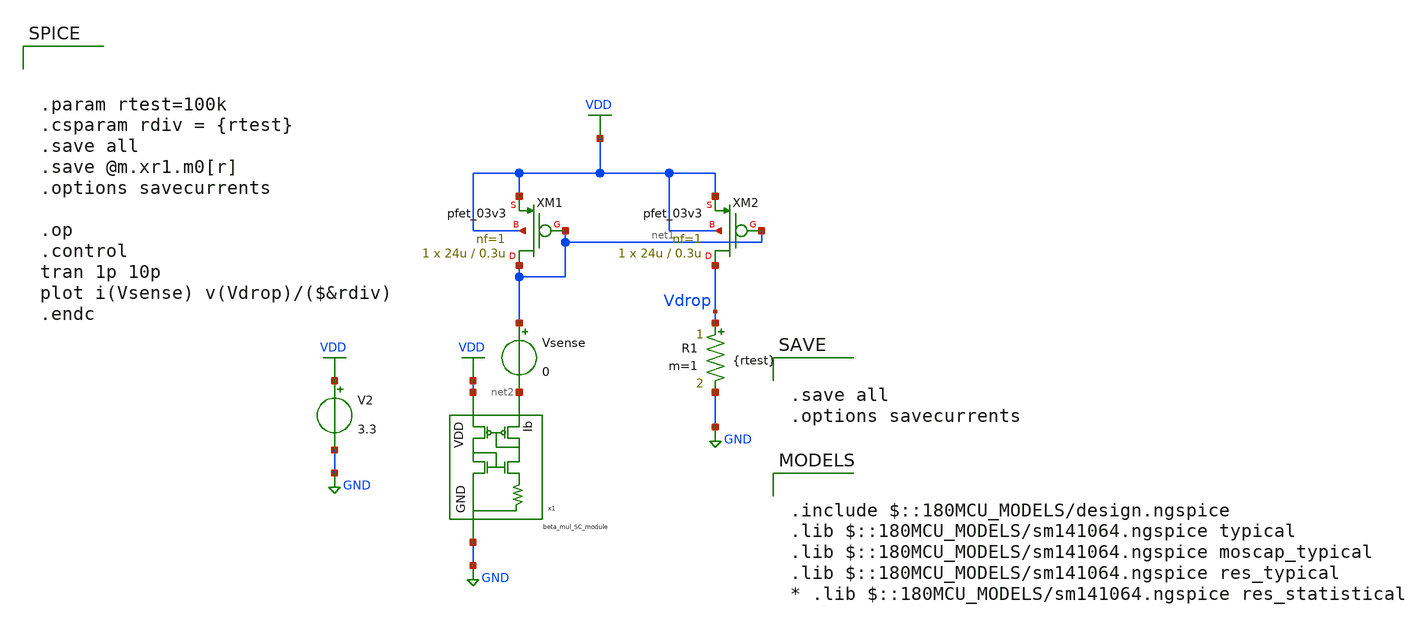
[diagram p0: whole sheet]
** sch_path: beta_mul_tb.sch
**.subckt beta_mul_tb
x1 VDD net2 GND beta_mul_SC_module
XM1 net1 net1 VDD VDD pfet_03v3 L=0.3u W=24u nf=1 ad='int((nf+1)/2) * W/nf * 0.18u' as='int((nf+2)/2) * W/nf * 0.18u'
+ pd='2*int((nf+1)/2) * (W/nf + 0.18u)' ps='2*int((nf+2)/2) * (W/nf + 0.18u)' nrd='0.18u / W' nrs='0.18u / W'
+ sa=0 sb=0 sd=0 m=1 par=1
XM2 Vdrop net1 VDD VDD pfet_03v3 L=0.3u W=24u nf=1 ad='int((nf+1)/2) * W/nf * 0.18u' as='int((nf+2)/2) * W/nf * 0.18u'
+ pd='2*int((nf+1)/2) * (W/nf + 0.18u)' ps='2*int((nf+2)/2) * (W/nf + 0.18u)' nrd='0.18u / W' nrs='0.18u / W'
+ sa=0 sb=0 sd=0 m=1 par=1
R1 Vdrop GND {rtest} m=1
Vsense net1 net2 0
V2 VDD GND 3.3
**** begin user architecture code

.include $::180MCU_MODELS/design.ngspice
.lib $::180MCU_MODELS/sm141064.ngspice typical
.lib $::180MCU_MODELS/sm141064.ngspice moscap_typical
.lib $::180MCU_MODELS/sm141064.ngspice res_typical
* .lib $::180MCU_MODELS/sm141064.ngspice res_statistical



.save all
.options savecurrents





.param rtest=100k
.csparam rdiv = {rtest}
.save all
.save @m.xr1.m0[r]
.options savecurrents

.op
.control
tran 1p 10p
plot i(Vsense) v(Vdrop)/($&rdiv)
.endc


**** end user architecture code
**.ends

* expanding   symbol:  beta_mul_SC_module.sym # of pins=3
** sym_path: beta_mul_SC_module.sym
** sch_path: beta_mul_SC_module.sch
.subckt beta_mul_SC_module VDD Ib GND
*.ipin VDD
*.ipin GND
*.ipin Ib
XM1 net1 Nbias GND GND nfet_03v3 L=0.6u W=15u nf=1 ad='int((nf+1)/2) * W/nf * 0.18u' as='int((nf+2)/2) * W/nf * 0.18u'
+ pd='2*int((nf+1)/2) * (W/nf + 0.18u)' ps='2*int((nf+2)/2) * (W/nf + 0.18u)' nrd='0.18u / W' nrs='0.18u / W'
+ sa=0 sb=0 sd=0 m=1 par=1
XM2 net1 net1 VDD VDD pfet_03v3 L=6u W=3u nf=1 ad='int((nf+1)/2) * W/nf * 0.18u' as='int((nf+2)/2) * W/nf * 0.18u'
+ pd='2*int((nf+1)/2) * (W/nf + 0.18u)' ps='2*int((nf+2)/2) * (W/nf + 0.18u)' nrd='0.18u / W' nrs='0.18u / W'
+ sa=0 sb=0 sd=0 m=1 par=1
XM3 Pbias net1 Nbias GND nfet_03v3 L=0.3u W=3u nf=1 ad='int((nf+1)/2) * W/nf * 0.18u' as='int((nf+2)/2) * W/nf * 0.18u'
+ pd='2*int((nf+1)/2) * (W/nf + 0.18u)' ps='2*int((nf+2)/2) * (W/nf + 0.18u)' nrd='0.18u / W' nrs='0.18u / W'
+ sa=0 sb=0 sd=0 m=1 par=1
XM4 Nbias Nbias GND GND nfet_03v3 L=0.6u W=15u nf=1 ad='int((nf+1)/2) * W/nf * 0.18u' as='int((nf+2)/2) * W/nf * 0.18u'
+ pd='2*int((nf+1)/2) * (W/nf + 0.18u)' ps='2*int((nf+2)/2) * (W/nf + 0.18u)' nrd='0.18u / W' nrs='0.18u / W'
+ sa=0 sb=0 sd=0 m=1 par=1
XM5 net3 net2 GND GND nfet_03v3 L=0.6u W=15u nf=1 ad='int((nf+1)/2) * W/nf * 0.18u' as='int((nf+2)/2) * W/nf * 0.18u'
+ pd='2*int((nf+1)/2) * (W/nf + 0.18u)' ps='2*int((nf+2)/2) * (W/nf + 0.18u)' nrd='0.18u / W' nrs='0.18u / W'
+ sa=0 sb=0 sd=0 m=1 par=1
XM6 Pbias Nbias GND GND nfet_03v3 L=0.6u W=15u nf=1 ad='int((nf+1)/2) * W/nf * 0.18u' as='int((nf+2)/2) * W/nf * 0.18u'
+ pd='2*int((nf+1)/2) * (W/nf + 0.18u)' ps='2*int((nf+2)/2) * (W/nf + 0.18u)' nrd='0.18u / W' nrs='0.18u / W'
+ sa=0 sb=0 sd=0 m=1 par=1
XM7 net2 net2 net4 GND nfet_03v3 L=0.6u W=60u nf=1 ad='int((nf+1)/2) * W/nf * 0.18u' as='int((nf+2)/2) * W/nf * 0.18u'
+ pd='2*int((nf+1)/2) * (W/nf + 0.18u)' ps='2*int((nf+2)/2) * (W/nf + 0.18u)' nrd='0.18u / W' nrs='0.18u / W'
+ sa=0 sb=0 sd=0 m=1 par=1
XM9 Nbias Pbias VDD VDD pfet_03v3 L=0.6u W=30u nf=1 ad='int((nf+1)/2) * W/nf * 0.18u' as='int((nf+2)/2) * W/nf * 0.18u'
+ pd='2*int((nf+1)/2) * (W/nf + 0.18u)' ps='2*int((nf+2)/2) * (W/nf + 0.18u)' nrd='0.18u / W' nrs='0.18u / W'
+ sa=0 sb=0 sd=0 m=1 par=1
XM10 net3 net3 VDD VDD pfet_03v3 L=0.6u W=30u nf=1 ad='int((nf+1)/2) * W/nf * 0.18u' as='int((nf+2)/2) * W/nf * 0.18u'
+ pd='2*int((nf+1)/2) * (W/nf + 0.18u)' ps='2*int((nf+2)/2) * (W/nf + 0.18u)' nrd='0.18u / W' nrs='0.18u / W'
+ sa=0 sb=0 sd=0 m=1 par=1
XM11 Pbias net3 VDD VDD pfet_03v3 L=0.6u W=30u nf=1 ad='int((nf+1)/2) * W/nf * 0.18u' as='int((nf+2)/2) * W/nf * 0.18u'
+ pd='2*int((nf+1)/2) * (W/nf + 0.18u)' ps='2*int((nf+2)/2) * (W/nf + 0.18u)' nrd='0.18u / W' nrs='0.18u / W'
+ sa=0 sb=0 sd=0 m=1 par=1
XM12 net2 Pbias VDD VDD pfet_03v3 L=0.6u W=30u nf=1 ad='int((nf+1)/2) * W/nf * 0.18u' as='int((nf+2)/2) * W/nf * 0.18u'
+ pd='2*int((nf+1)/2) * (W/nf + 0.18u)' ps='2*int((nf+2)/2) * (W/nf + 0.18u)' nrd='0.18u / W' nrs='0.18u / W'
+ sa=0 sb=0 sd=0 m=1 par=1
XM8 Ib Nbias GND GND nfet_03v3 L=0.6u W=7.5u nf=1 ad='int((nf+1)/2) * W/nf * 0.18u' as='int((nf+2)/2) * W/nf * 0.18u'
+ pd='2*int((nf+1)/2) * (W/nf + 0.18u)' ps='2*int((nf+2)/2) * (W/nf + 0.18u)' nrd='0.18u / W' nrs='0.18u / W'
+ sa=0 sb=0 sd=0 m=1 par=1
XC1 Nbias GND cap_nmos_03v3 c_width=20u c_length=20u m=1
XC2 Pbias VDD cap_pmos_03v3 c_width=20u c_length=20u m=1
XR1 GND net4 GND npolyf_u r_width=5u r_length=52.5u m=1
.ends

.GLOBAL VDD
.GLOBAL GND
.end
